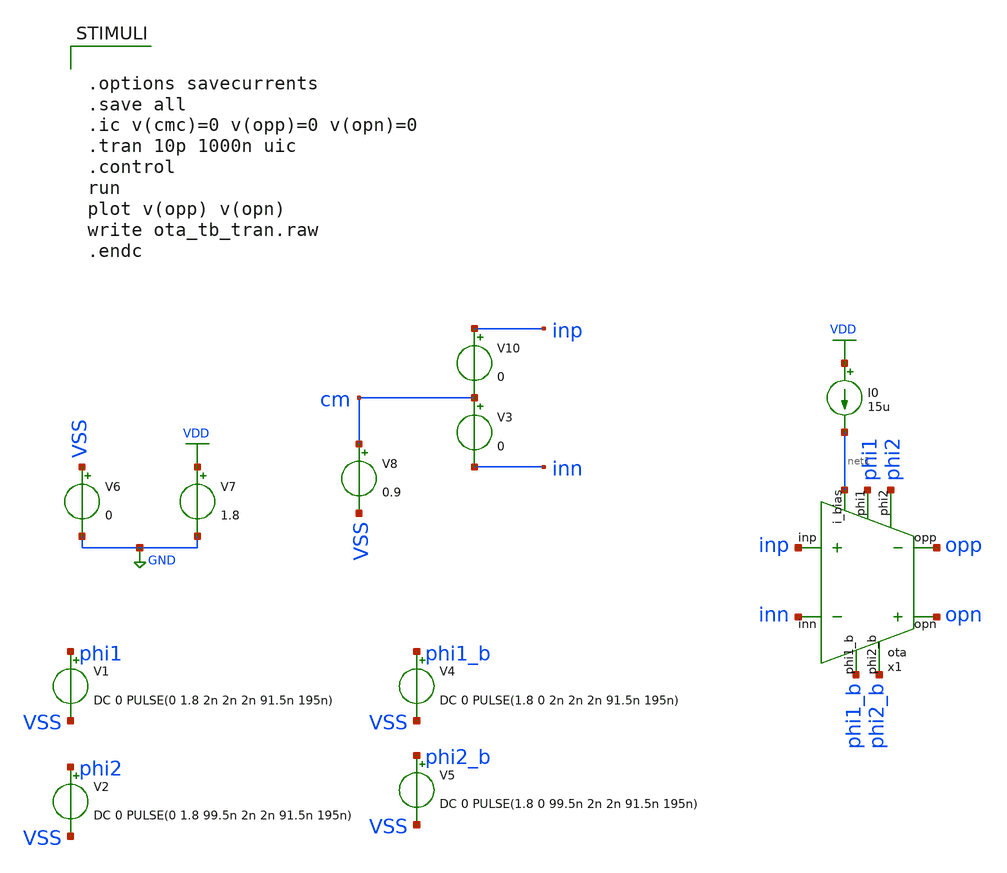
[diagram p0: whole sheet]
** sch_path: verification/schematic/ota_tb_tran.sch
**.subckt ota_tb_tran
V6 VSS GND 0
V7 VDD GND 1.8
V8 cm VSS 0.9
V1 phi1 VSS DC 0 PULSE(0 1.8 2n 2n 2n 91.5n 195n)
V2 phi2 VSS DC 0 PULSE(0 1.8 99.5n 2n 2n 91.5n 195n)
V4 phi1_b VSS DC 0 PULSE(1.8 0 2n 2n 2n 91.5n 195n)
V5 phi2_b VSS DC 0 PULSE(1.8 0 99.5n 2n 2n 91.5n 195n)
x1 net1 inp inn phi1 phi1_b phi2 phi2_b opp opn 50 350 VDD VSS ota
I0 VDD net1 15u
V10 inp cm 0
V3 cm inn 0
**** begin user architecture code

** opencircuitdesign pdks install
.lib /farmshare/home/classes/ee/372/PDKs/open_pdks_1.0.310/sky130/sky130A/libs.tech/ngspice/sky130.lib.spice tt



.options savecurrents
.save all
.ic v(cmc)=0 v(opp)=0 v(opn)=0
.tran 10p 1000n uic
.control
run
plot v(opp) v(opn)
write ota_tb_tran.raw
.endc


**** end user architecture code
**.ends
.GLOBAL VDD
.GLOBAL GND
.end
